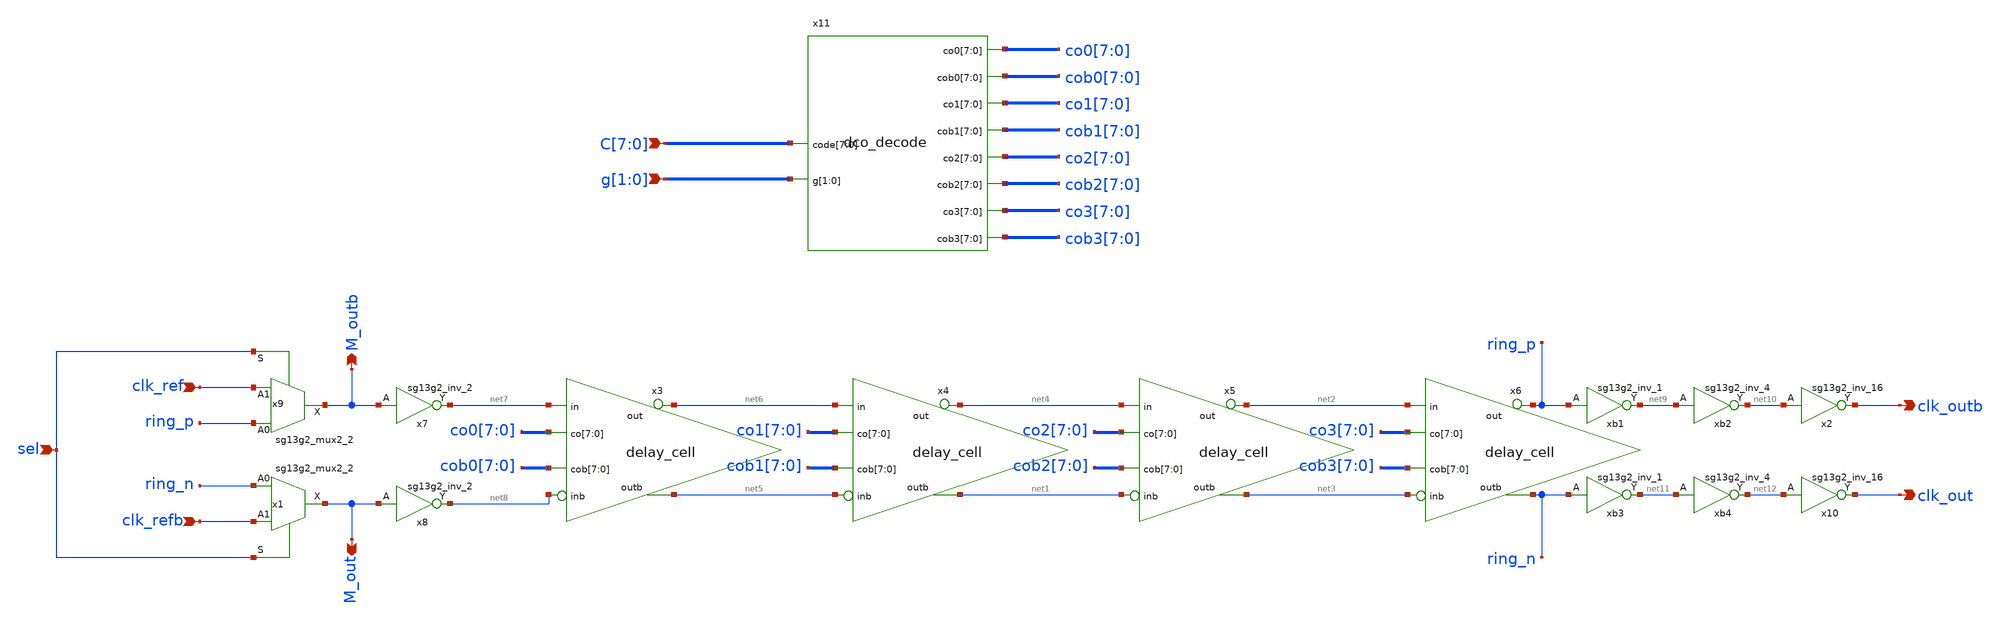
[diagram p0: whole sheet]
** sch_path: TPU5555-main/mdll/mixed_signal_design_blocks/clk_gen/src/dco.sch
* IHP-GmbH/IHP-Open-PDK/ihp-sg13g2/libs.tech/xschem/sg13g2_stdcells/sg13g2_inv_16.sch:
* Copyright 2023 IHP PDK Authors
* Licensed under the Apache License, Version 2.0 (the "License");
**.subckt dco clk_refb clk_ref sel clk_outb M_out M_outb clk_out
*+ C[7],C[6],C[5],C[4],C[3],C[2],C[1],C[0] g[1],g[0]
*.ipin clk_refb
*.ipin clk_ref
*.ipin sel
*.opin clk_outb
*.opin M_out
*.opin M_outb
*.opin clk_out
*.ipin C[7],C[6],C[5],C[4],C[3],C[2],C[1],C[0]
*.ipin g[1],g[0]
x3 net7 net6 co0[7] co0[6] co0[5] co0[4] co0[3] co0[2] co0[1] co0[0] cob0[7] cob0[6] cob0[5] cob0[4]
+ cob0[3] cob0[2] cob0[1] cob0[0] net5 net8 delay_cell
x4 net6 net4 co1[7] co1[6] co1[5] co1[4] co1[3] co1[2] co1[1] co1[0] cob1[7] cob1[6] cob1[5] cob1[4]
+ cob1[3] cob1[2] cob1[1] cob1[0] net1 net5 delay_cell
x5 net4 net2 co2[7] co2[6] co2[5] co2[4] co2[3] co2[2] co2[1] co2[0] cob2[7] cob2[6] cob2[5] cob2[4]
+ cob2[3] cob2[2] cob2[1] cob2[0] net3 net1 delay_cell
x6 net2 ring_p co3[7] co3[6] co3[5] co3[4] co3[3] co3[2] co3[1] co3[0] cob3[7] cob3[6] cob3[5]
+ cob3[4] cob3[3] cob3[2] cob3[1] cob3[0] ring_n net3 delay_cell
x7 net7 M_outb VDD VSS sg13g2_inv_2
x8 net8 M_out VDD VSS sg13g2_inv_2
x9 M_outb ring_p clk_ref sel VDD VSS sg13g2_mux2_2
x1 M_out ring_n clk_refb sel VDD VSS sg13g2_mux2_2
x2 clk_outb net10 VDD VSS sg13g2_inv_16
x10 clk_out net12 VDD VSS sg13g2_inv_16
x11 C[7] C[6] C[5] C[4] C[3] C[2] C[1] C[0] g[1] g[0] co0[7] co0[6] co0[5] co0[4] co0[3] co0[2]
+ co0[1] co0[0] cob0[7] cob0[6] cob0[5] cob0[4] cob0[3] cob0[2] cob0[1] cob0[0] co1[7] co1[6] co1[5] co1[4]
+ co1[3] co1[2] co1[1] co1[0] cob1[7] cob1[6] cob1[5] cob1[4] cob1[3] cob1[2] cob1[1] cob1[0] co2[7] co2[6]
+ co2[5] co2[4] co2[3] co2[2] co2[1] co2[0] cob2[7] cob2[6] cob2[5] cob2[4] cob2[3] cob2[2] cob2[1] cob2[0]
+ co3[7] co3[6] co3[5] co3[4] co3[3] co3[2] co3[1] co3[0] cob3[7] cob3[6] cob3[5] cob3[4] cob3[3] cob3[2]
+ cob3[1] cob3[0] dco_decode
xb1 net9 ring_p VDD VSS sg13g2_inv_1
xb2 net10 net9 VDD VSS sg13g2_inv_4
xb3 net11 ring_n VDD VSS sg13g2_inv_1
xb4 net12 net11 VDD VSS sg13g2_inv_4
**.ends

* expanding   symbol:  clk_gen/src/delay_cell.sym # of pins=6
** sym_path: TPU5555-main/mdll/mixed_signal_design_blocks/clk_gen/src/delay_cell.sym
** sch_path: TPU5555-main/mdll/mixed_signal_design_blocks/clk_gen/src/delay_cell.sch
.subckt delay_cell in out co[7] co[6] co[5] co[4] co[3] co[2] co[1] co[0] cob[7] cob[6] cob[5]
+ cob[4] cob[3] cob[2] cob[1] cob[0] outb inb
*.ipin in
*.ipin inb
*.opin out
*.opin outb
*.ipin co[7],co[6],co[5],co[4],co[3],co[2],co[1],co[0]
*.ipin cob[7],cob[6],cob[5],cob[4],cob[3],cob[2],cob[1],cob[0]
x13 out in VDD VSS sg13g2_inv_2
x14 outb inb VDD VSS sg13g2_inv_2
x11 out outb VDD VSS sg13g2_inv_1
x12 outb out VDD VSS sg13g2_inv_1
xco0 co[0] out VDD VSS custom_cap_8
* tap: co[7:0] --> co[0]
xco1 co[1] out VDD VSS custom_cap_8
* tap: co[7:0] --> co[1]
xco2 co[2] out VDD VSS custom_cap_8
* tap: co[7:0] --> co[2]
xco3 co[3] out VDD VSS custom_cap_8
* tap: co[7:0] --> co[3]
xco4 co[4] out VDD VSS custom_cap_8
* tap: co[7:0] --> co[4]
xco5 co[5] out VDD VSS custom_cap_8
* tap: co[7:0] --> co[5]
xco6 co[6] out VDD VSS custom_cap_8
* tap: co[7:0] --> co[6]
xco7 co[7] out VDD VSS custom_cap_8
* tap: co[7:0] --> co[7]
xcob0 cob[0] outb VDD VSS custom_cap_8
* tap: cob[7:0] --> cob[0]
xcob1 cob[1] outb VDD VSS custom_cap_8
* tap: cob[7:0] --> cob[1]
xcob2 cob[2] outb VDD VSS custom_cap_8
* tap: cob[7:0] --> cob[2]
xcob3 cob[3] outb VDD VSS custom_cap_8
* tap: cob[7:0] --> cob[3]
xcob4 cob[4] outb VDD VSS custom_cap_8
* tap: cob[7:0] --> cob[4]
xcob5 cob[5] outb VDD VSS custom_cap_8
* tap: cob[7:0] --> cob[5]
xcob6 cob[6] outb VDD VSS custom_cap_8
* tap: cob[7:0] --> cob[6]
xcob7 cob[7] outb VDD VSS custom_cap_8
* tap: cob[7:0] --> cob[7]
.ends


* expanding   symbol:  sg13g2_inv_2.sym # of pins=2
** sym_path: sg13g2_inv_2.sym
** sch_path: sg13g2_inv_2.sch
.subckt sg13g2_inv_2 Y A VDD VSS
*.opin Y
*.ipin A
*.iopin VDD
*.iopin VSS
XM1 Y A VSS VSS sg13_lv_nmos w=1.48u l=130.00n ng=2 m=1 mm_ok=1
XM2 Y A VDD VDD sg13_lv_pmos w=2.24u l=130.00n ng=2 m=1 mm_ok=1
.ends


* expanding   symbol:  sg13g2_mux2_2.sym # of pins=4
** sym_path: sg13g2_mux2_2.sym
** sch_path: sg13g2_mux2_2.sch
.subckt sg13g2_mux2_2 X A0 A1 S VDD VSS
*.ipin S
*.ipin A0
*.ipin A1
*.opin X
*.iopin VDD
*.iopin VSS
XM1 Sb S VSS VSS sg13_lv_nmos w=550.00n l=130.00n ng=1 m=1 mm_ok=1
XM2 net1 A0 net5 VSS sg13_lv_nmos w=740.00n l=130.00n ng=1 m=1 mm_ok=1
XM3 net5 Sb VSS VSS sg13_lv_nmos w=740.00n l=130.00n ng=1 m=1 mm_ok=1
XM4 net1 A1 net4 VSS sg13_lv_nmos w=740.00n l=130.00n ng=1 m=1 mm_ok=1
XM5 net4 S VSS VSS sg13_lv_nmos w=740.00n l=130.00n ng=1 m=1 mm_ok=1
XM6 X net1 VSS VSS sg13_lv_nmos w=1.48u l=130.00n ng=2 m=1 mm_ok=1
XM7 Sb S VDD VDD sg13_lv_pmos w=840.00n l=130.00n ng=1 m=1 mm_ok=1
XM8 net2 S VDD VDD sg13_lv_pmos w=1.000u l=130.00n ng=1 m=1 mm_ok=1
XM9 net1 A0 net2 VDD sg13_lv_pmos w=1.000u l=130.00n ng=1 m=1 mm_ok=1
XM10 net3 Sb VDD VDD sg13_lv_pmos w=1.000u l=130.00n ng=1 m=1 mm_ok=1
XM11 net1 A1 net3 VDD sg13_lv_pmos w=1.000u l=130.00n ng=1 m=1 mm_ok=1
XM12 X net1 VDD VDD sg13_lv_pmos w=2.24u l=130.00n ng=2 m=1 mm_ok=1
.ends


* expanding   symbol:  sg13g2_inv_16.sym # of pins=2
** sym_path: sg13g2_inv_16.sym
** sch_path: sg13g2_inv_16.sch
.subckt sg13g2_inv_16 Y A VDD VSS
*.opin Y
*.iopin VSS
*.ipin A
*.iopin VDD
XM1 Y A VSS VSS sg13_lv_nmos w=11.84u l=130.00n ng=16 m=1 mm_ok=1
XM2 Y A VDD VDD sg13_lv_pmos w=17.92u l=130.00n ng=16 m=1 mm_ok=1
.ends


* expanding   symbol:  sg13g2_inv_1.sym # of pins=2
** sym_path: sg13g2_inv_1.sym
** sch_path: sg13g2_inv_1.sch
.subckt sg13g2_inv_1 Y A VDD VSS
*.opin Y
*.ipin A
*.iopin VDD
*.iopin VSS
XM1 Y A VSS VSS sg13_lv_nmos w=740.00n l=130.00n ng=1 m=1 mm_ok=1
XM2 Y A VDD VDD sg13_lv_pmos w=1.12u l=130.00n ng=1 m=1 mm_ok=1
.ends


* expanding   symbol:  sg13g2_inv_4.sym # of pins=2
** sym_path: sg13g2_inv_4.sym
** sch_path: sg13g2_inv_4.sch
.subckt sg13g2_inv_4 Y A VDD VSS
*.ipin A
*.opin Y
*.iopin VDD
*.iopin VSS
XM1 Y A VSS VSS sg13_lv_nmos w=2.96u l=130.00n ng=4 m=1 mm_ok=1
XM2 Y A VDD VDD sg13_lv_pmos w=4.48u l=130.00n ng=4 m=1 mm_ok=1
.ends

.end
